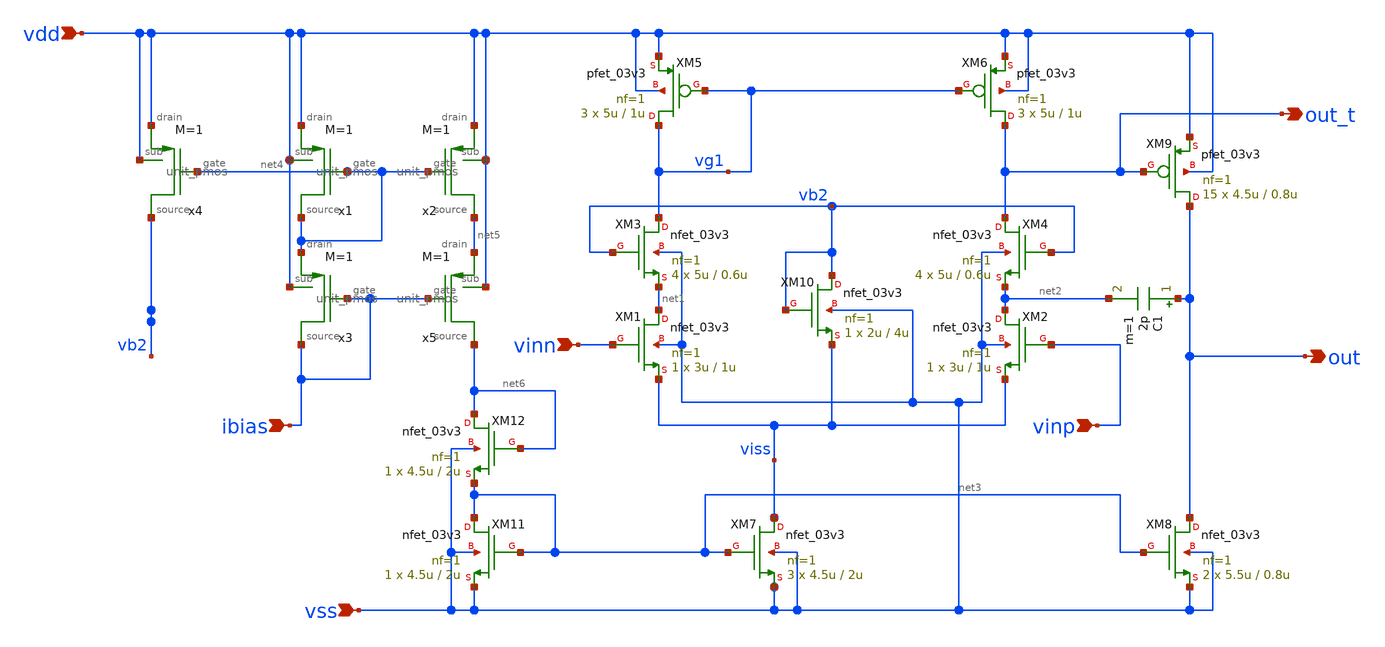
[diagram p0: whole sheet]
** sch_path: designs/libs/core_analog/opamp/opamp_n_input.sch
**.subckt opamp_n_input out vdd vss vinn ibias vinp out_t
*.opin out
*.ipin vdd
*.ipin vss
*.ipin vinn
*.ipin ibias
*.ipin vinp
*.opin out_t
XM1 net1 vinn viss vss nfet_03v3 L=1u W=3u nf=1 ad='int((nf+1)/2) * W/nf * 0.18u' as='int((nf+2)/2) * W/nf * 0.18u'
+ pd='2*int((nf+1)/2) * (W/nf + 0.18u)' ps='2*int((nf+2)/2) * (W/nf + 0.18u)' nrd='0.18u / W' nrs='0.18u / W'
+ sa=0 sb=0 sd=0 m=1
XM2 net2 vinp viss vss nfet_03v3 L=1u W=3u nf=1 ad='int((nf+1)/2) * W/nf * 0.18u' as='int((nf+2)/2) * W/nf * 0.18u'
+ pd='2*int((nf+1)/2) * (W/nf + 0.18u)' ps='2*int((nf+2)/2) * (W/nf + 0.18u)' nrd='0.18u / W' nrs='0.18u / W'
+ sa=0 sb=0 sd=0 m=1
XM6 out_t vg1 vdd vdd pfet_03v3 L=1u W=5u nf=1 ad='int((nf+1)/2) * W/nf * 0.18u' as='int((nf+2)/2) * W/nf * 0.18u'
+ pd='2*int((nf+1)/2) * (W/nf + 0.18u)' ps='2*int((nf+2)/2) * (W/nf + 0.18u)' nrd='0.18u / W' nrs='0.18u / W'
+ sa=0 sb=0 sd=0 m=3
XM5 vg1 vg1 vdd vdd pfet_03v3 L=1u W=5u nf=1 ad='int((nf+1)/2) * W/nf * 0.18u' as='int((nf+2)/2) * W/nf * 0.18u'
+ pd='2*int((nf+1)/2) * (W/nf + 0.18u)' ps='2*int((nf+2)/2) * (W/nf + 0.18u)' nrd='0.18u / W' nrs='0.18u / W'
+ sa=0 sb=0 sd=0 m=3
XM4 out_t vb2 net2 vss nfet_03v3 L=0.6u W=5u nf=1 ad='int((nf+1)/2) * W/nf * 0.18u' as='int((nf+2)/2) * W/nf * 0.18u'
+ pd='2*int((nf+1)/2) * (W/nf + 0.18u)' ps='2*int((nf+2)/2) * (W/nf + 0.18u)' nrd='0.18u / W' nrs='0.18u / W'
+ sa=0 sb=0 sd=0 m=4
XM3 vg1 vb2 net1 vss nfet_03v3 L=0.6u W=5u nf=1 ad='int((nf+1)/2) * W/nf * 0.18u' as='int((nf+2)/2) * W/nf * 0.18u'
+ pd='2*int((nf+1)/2) * (W/nf + 0.18u)' ps='2*int((nf+2)/2) * (W/nf + 0.18u)' nrd='0.18u / W' nrs='0.18u / W'
+ sa=0 sb=0 sd=0 m=4
XM7 viss net3 vss vss nfet_03v3 L=2u W=4.5u nf=1 ad='int((nf+1)/2) * W/nf * 0.18u' as='int((nf+2)/2) * W/nf * 0.18u'
+ pd='2*int((nf+1)/2) * (W/nf + 0.18u)' ps='2*int((nf+2)/2) * (W/nf + 0.18u)' nrd='0.18u / W' nrs='0.18u / W'
+ sa=0 sb=0 sd=0 m=3
XM11 net3 net3 vss vss nfet_03v3 L=2u W=4.5u nf=1 ad='int((nf+1)/2) * W/nf * 0.18u' as='int((nf+2)/2) * W/nf * 0.18u'
+ pd='2*int((nf+1)/2) * (W/nf + 0.18u)' ps='2*int((nf+2)/2) * (W/nf + 0.18u)' nrd='0.18u / W' nrs='0.18u / W'
+ sa=0 sb=0 sd=0 m=1
x1 vdd vdd net4 net4 unit_pmos M=1
x2 vdd vdd net4 net5 unit_pmos M=1
x4 vdd vdd net4 vb2 unit_pmos M=1
x3 net4 vdd ibias ibias unit_pmos M=1
x5 net5 vdd ibias net6 unit_pmos M=1
XM10 vb2 vb2 viss vss nfet_03v3 L=4u W=2u nf=1 ad='int((nf+1)/2) * W/nf * 0.18u' as='int((nf+2)/2) * W/nf * 0.18u'
+ pd='2*int((nf+1)/2) * (W/nf + 0.18u)' ps='2*int((nf+2)/2) * (W/nf + 0.18u)' nrd='0.18u / W' nrs='0.18u / W'
+ sa=0 sb=0 sd=0 m=1
C1 out net2 2p m=1
XM8 out net3 vss vss nfet_03v3 L=0.8u W=5.5u nf=1 ad='int((nf+1)/2) * W/nf * 0.18u' as='int((nf+2)/2) * W/nf * 0.18u'
+ pd='2*int((nf+1)/2) * (W/nf + 0.18u)' ps='2*int((nf+2)/2) * (W/nf + 0.18u)' nrd='0.18u / W' nrs='0.18u / W'
+ sa=0 sb=0 sd=0 m=2
XM9 out out_t vdd vdd pfet_03v3 L=0.8u W=4.5u nf=1 ad='int((nf+1)/2) * W/nf * 0.18u' as='int((nf+2)/2) * W/nf * 0.18u'
+ pd='2*int((nf+1)/2) * (W/nf + 0.18u)' ps='2*int((nf+2)/2) * (W/nf + 0.18u)' nrd='0.18u / W' nrs='0.18u / W'
+ sa=0 sb=0 sd=0 m=15
XM12 net6 net6 net3 vss nfet_03v3 L=2u W=4.5u nf=1 ad='int((nf+1)/2) * W/nf * 0.18u' as='int((nf+2)/2) * W/nf * 0.18u'
+ pd='2*int((nf+1)/2) * (W/nf + 0.18u)' ps='2*int((nf+2)/2) * (W/nf + 0.18u)' nrd='0.18u / W' nrs='0.18u / W'
+ sa=0 sb=0 sd=0 m=1
**.ends

* expanding   symbol:  libs/core_analog/unit_pmos/unit_pmos.sym # of pins=4
** sym_path: libs/core_analog/unit_pmos/unit_pmos.sym
** sch_path: libs/core_analog/unit_pmos/unit_pmos.sch
.subckt unit_pmos drain sub gate source
*.iopin drain
*.iopin source
*.iopin sub
*.iopin gate
**** begin user architecture code

.param M=1

**** end user architecture code
XM3 drain gate source sub pfet_03v3 L=1u W=3.5u nf=1 ad='int((nf+1)/2) * W/nf * 0.18u' as='int((nf+2)/2) * W/nf * 0.18u'
+ pd='2*int((nf+1)/2) * (W/nf + 0.18u)' ps='2*int((nf+2)/2) * (W/nf + 0.18u)' nrd='0.18u / W' nrs='0.18u / W'
+ sa=0 sb=0 sd=0 m={M}
.ends

.end
